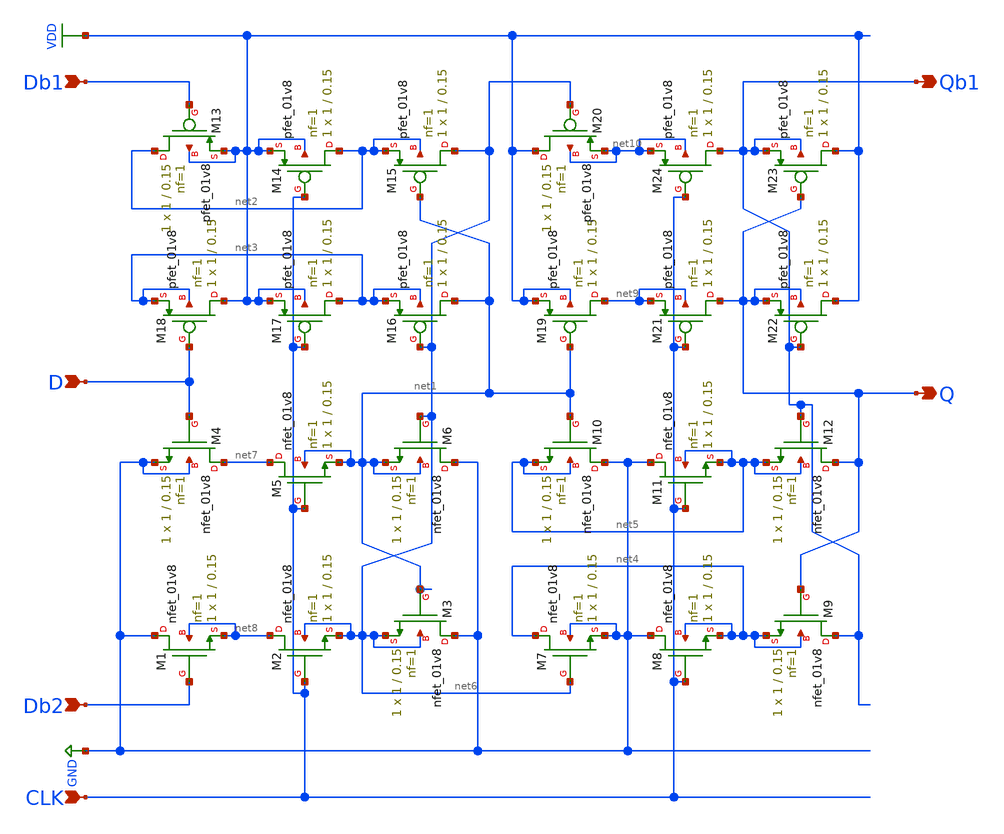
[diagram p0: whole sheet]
** sch_path: projects/negdff/xschem_ngspice/negdff2.sch
**.subckt negdff2 D Db1 Db2 Q Qb1 CLK
*.ipin D
*.ipin Db1
*.ipin Db2
*.opin Q
*.opin Qb1
*.ipin CLK
XM1 GND Db2 net8 net8 sky130_fd_pr__nfet_01v8 L=0.15 W=1 nf=1 ad='int((nf+1)/2) * W/nf * 0.29' as='int((nf+2)/2) * W/nf * 0.29'
+ pd='2*int((nf+1)/2) * (W/nf + 0.29)' ps='2*int((nf+2)/2) * (W/nf + 0.29)' nrd='0.29 / W' nrs='0.29 / W'
+ sa=0 sb=0 sd=0 mult=1 m=1
XM2 net8 CLK net6 net6 sky130_fd_pr__nfet_01v8 L=0.15 W=1 nf=1 ad='int((nf+1)/2) * W/nf * 0.29' as='int((nf+2)/2) * W/nf * 0.29'
+ pd='2*int((nf+1)/2) * (W/nf + 0.29)' ps='2*int((nf+2)/2) * (W/nf + 0.29)' nrd='0.29 / W' nrs='0.29 / W'
+ sa=0 sb=0 sd=0 mult=1 m=1
XM3 GND net1 net6 net6 sky130_fd_pr__nfet_01v8 L=0.15 W=1 nf=1 ad='int((nf+1)/2) * W/nf * 0.29' as='int((nf+2)/2) * W/nf * 0.29'
+ pd='2*int((nf+1)/2) * (W/nf + 0.29)' ps='2*int((nf+2)/2) * (W/nf + 0.29)' nrd='0.29 / W' nrs='0.29 / W'
+ sa=0 sb=0 sd=0 mult=1 m=1
XM4 net7 D GND GND sky130_fd_pr__nfet_01v8 L=0.15 W=1 nf=1 ad='int((nf+1)/2) * W/nf * 0.29' as='int((nf+2)/2) * W/nf * 0.29'
+ pd='2*int((nf+1)/2) * (W/nf + 0.29)' ps='2*int((nf+2)/2) * (W/nf + 0.29)' nrd='0.29 / W' nrs='0.29 / W'
+ sa=0 sb=0 sd=0 mult=1 m=1
XM5 net7 CLK net1 net1 sky130_fd_pr__nfet_01v8 L=0.15 W=1 nf=1 ad='int((nf+1)/2) * W/nf * 0.29' as='int((nf+2)/2) * W/nf * 0.29'
+ pd='2*int((nf+1)/2) * (W/nf + 0.29)' ps='2*int((nf+2)/2) * (W/nf + 0.29)' nrd='0.29 / W' nrs='0.29 / W'
+ sa=0 sb=0 sd=0 mult=1 m=1
XM6 GND net6 net1 net1 sky130_fd_pr__nfet_01v8 L=0.15 W=1 nf=1 ad='int((nf+1)/2) * W/nf * 0.29' as='int((nf+2)/2) * W/nf * 0.29'
+ pd='2*int((nf+1)/2) * (W/nf + 0.29)' ps='2*int((nf+2)/2) * (W/nf + 0.29)' nrd='0.29 / W' nrs='0.29 / W'
+ sa=0 sb=0 sd=0 mult=1 m=1
XM7 net4 net6 GND GND sky130_fd_pr__nfet_01v8 L=0.15 W=1 nf=1 ad='int((nf+1)/2) * W/nf * 0.29' as='int((nf+2)/2) * W/nf * 0.29'
+ pd='2*int((nf+1)/2) * (W/nf + 0.29)' ps='2*int((nf+2)/2) * (W/nf + 0.29)' nrd='0.29 / W' nrs='0.29 / W'
+ sa=0 sb=0 sd=0 mult=1 m=1
XM8 GND CLK net4 net4 sky130_fd_pr__nfet_01v8 L=0.15 W=1 nf=1 ad='int((nf+1)/2) * W/nf * 0.29' as='int((nf+2)/2) * W/nf * 0.29'
+ pd='2*int((nf+1)/2) * (W/nf + 0.29)' ps='2*int((nf+2)/2) * (W/nf + 0.29)' nrd='0.29 / W' nrs='0.29 / W'
+ sa=0 sb=0 sd=0 mult=1 m=1
XM9 Qb1 Q net4 net4 sky130_fd_pr__nfet_01v8 L=0.15 W=1 nf=1 ad='int((nf+1)/2) * W/nf * 0.29' as='int((nf+2)/2) * W/nf * 0.29'
+ pd='2*int((nf+1)/2) * (W/nf + 0.29)' ps='2*int((nf+2)/2) * (W/nf + 0.29)' nrd='0.29 / W' nrs='0.29 / W'
+ sa=0 sb=0 sd=0 mult=1 m=1
XM10 GND net1 net5 net5 sky130_fd_pr__nfet_01v8 L=0.15 W=1 nf=1 ad='int((nf+1)/2) * W/nf * 0.29' as='int((nf+2)/2) * W/nf * 0.29'
+ pd='2*int((nf+1)/2) * (W/nf + 0.29)' ps='2*int((nf+2)/2) * (W/nf + 0.29)' nrd='0.29 / W' nrs='0.29 / W'
+ sa=0 sb=0 sd=0 mult=1 m=1
XM11 GND CLK net5 net5 sky130_fd_pr__nfet_01v8 L=0.15 W=1 nf=1 ad='int((nf+1)/2) * W/nf * 0.29' as='int((nf+2)/2) * W/nf * 0.29'
+ pd='2*int((nf+1)/2) * (W/nf + 0.29)' ps='2*int((nf+2)/2) * (W/nf + 0.29)' nrd='0.29 / W' nrs='0.29 / W'
+ sa=0 sb=0 sd=0 mult=1 m=1
XM12 Q Qb1 net5 net5 sky130_fd_pr__nfet_01v8 L=0.15 W=1 nf=1 ad='int((nf+1)/2) * W/nf * 0.29' as='int((nf+2)/2) * W/nf * 0.29'
+ pd='2*int((nf+1)/2) * (W/nf + 0.29)' ps='2*int((nf+2)/2) * (W/nf + 0.29)' nrd='0.29 / W' nrs='0.29 / W'
+ sa=0 sb=0 sd=0 mult=1 m=1
XM13 net2 Db1 VDD VDD sky130_fd_pr__pfet_01v8 L=0.15 W=1 nf=1 ad='int((nf+1)/2) * W/nf * 0.29' as='int((nf+2)/2) * W/nf * 0.29'
+ pd='2*int((nf+1)/2) * (W/nf + 0.29)' ps='2*int((nf+2)/2) * (W/nf + 0.29)' nrd='0.29 / W' nrs='0.29 / W'
+ sa=0 sb=0 sd=0 mult=1 m=1
XM14 net2 CLK VDD VDD sky130_fd_pr__pfet_01v8 L=0.15 W=1 nf=1 ad='int((nf+1)/2) * W/nf * 0.29' as='int((nf+2)/2) * W/nf * 0.29'
+ pd='2*int((nf+1)/2) * (W/nf + 0.29)' ps='2*int((nf+2)/2) * (W/nf + 0.29)' nrd='0.29 / W' nrs='0.29 / W'
+ sa=0 sb=0 sd=0 mult=1 m=1
XM15 net6 net1 net2 net2 sky130_fd_pr__pfet_01v8 L=0.15 W=1 nf=1 ad='int((nf+1)/2) * W/nf * 0.29' as='int((nf+2)/2) * W/nf * 0.29'
+ pd='2*int((nf+1)/2) * (W/nf + 0.29)' ps='2*int((nf+2)/2) * (W/nf + 0.29)' nrd='0.29 / W' nrs='0.29 / W'
+ sa=0 sb=0 sd=0 mult=1 m=1
XM16 net1 net6 net3 net3 sky130_fd_pr__pfet_01v8 L=0.15 W=1 nf=1 ad='int((nf+1)/2) * W/nf * 0.29' as='int((nf+2)/2) * W/nf * 0.29'
+ pd='2*int((nf+1)/2) * (W/nf + 0.29)' ps='2*int((nf+2)/2) * (W/nf + 0.29)' nrd='0.29 / W' nrs='0.29 / W'
+ sa=0 sb=0 sd=0 mult=1 m=1
XM17 net3 CLK VDD VDD sky130_fd_pr__pfet_01v8 L=0.15 W=1 nf=1 ad='int((nf+1)/2) * W/nf * 0.29' as='int((nf+2)/2) * W/nf * 0.29'
+ pd='2*int((nf+1)/2) * (W/nf + 0.29)' ps='2*int((nf+2)/2) * (W/nf + 0.29)' nrd='0.29 / W' nrs='0.29 / W'
+ sa=0 sb=0 sd=0 mult=1 m=1
XM18 VDD D net3 net3 sky130_fd_pr__pfet_01v8 L=0.15 W=1 nf=1 ad='int((nf+1)/2) * W/nf * 0.29' as='int((nf+2)/2) * W/nf * 0.29'
+ pd='2*int((nf+1)/2) * (W/nf + 0.29)' ps='2*int((nf+2)/2) * (W/nf + 0.29)' nrd='0.29 / W' nrs='0.29 / W'
+ sa=0 sb=0 sd=0 mult=1 m=1
XM19 net9 net1 VDD VDD sky130_fd_pr__pfet_01v8 L=0.15 W=1 nf=1 ad='int((nf+1)/2) * W/nf * 0.29' as='int((nf+2)/2) * W/nf * 0.29'
+ pd='2*int((nf+1)/2) * (W/nf + 0.29)' ps='2*int((nf+2)/2) * (W/nf + 0.29)' nrd='0.29 / W' nrs='0.29 / W'
+ sa=0 sb=0 sd=0 mult=1 m=1
XM20 VDD net6 net10 net10 sky130_fd_pr__pfet_01v8 L=0.15 W=1 nf=1 ad='int((nf+1)/2) * W/nf * 0.29' as='int((nf+2)/2) * W/nf * 0.29'
+ pd='2*int((nf+1)/2) * (W/nf + 0.29)' ps='2*int((nf+2)/2) * (W/nf + 0.29)' nrd='0.29 / W' nrs='0.29 / W'
+ sa=0 sb=0 sd=0 mult=1 m=1
XM21 Q CLK net9 net9 sky130_fd_pr__pfet_01v8 L=0.15 W=1 nf=1 ad='int((nf+1)/2) * W/nf * 0.29' as='int((nf+2)/2) * W/nf * 0.29'
+ pd='2*int((nf+1)/2) * (W/nf + 0.29)' ps='2*int((nf+2)/2) * (W/nf + 0.29)' nrd='0.29 / W' nrs='0.29 / W'
+ sa=0 sb=0 sd=0 mult=1 m=1
XM22 VDD Qb1 Q Q sky130_fd_pr__pfet_01v8 L=0.15 W=1 nf=1 ad='int((nf+1)/2) * W/nf * 0.29' as='int((nf+2)/2) * W/nf * 0.29'
+ pd='2*int((nf+1)/2) * (W/nf + 0.29)' ps='2*int((nf+2)/2) * (W/nf + 0.29)' nrd='0.29 / W' nrs='0.29 / W'
+ sa=0 sb=0 sd=0 mult=1 m=1
XM23 VDD Q Qb1 Qb1 sky130_fd_pr__pfet_01v8 L=0.15 W=1 nf=1 ad='int((nf+1)/2) * W/nf * 0.29' as='int((nf+2)/2) * W/nf * 0.29'
+ pd='2*int((nf+1)/2) * (W/nf + 0.29)' ps='2*int((nf+2)/2) * (W/nf + 0.29)' nrd='0.29 / W' nrs='0.29 / W'
+ sa=0 sb=0 sd=0 mult=1 m=1
XM24 Qb1 CLK net10 net10 sky130_fd_pr__pfet_01v8 L=0.15 W=1 nf=1 ad='int((nf+1)/2) * W/nf * 0.29' as='int((nf+2)/2) * W/nf * 0.29'
+ pd='2*int((nf+1)/2) * (W/nf + 0.29)' ps='2*int((nf+2)/2) * (W/nf + 0.29)' nrd='0.29 / W' nrs='0.29 / W'
+ sa=0 sb=0 sd=0 mult=1 m=1
**.ends
.GLOBAL GND
.GLOBAL VDD
.end
